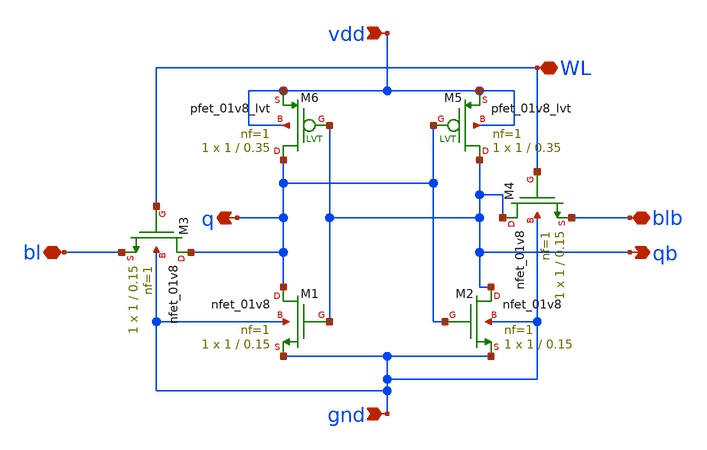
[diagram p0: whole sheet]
** sch_path: sram.sch
**.subckt sram vdd bl q gnd WL blb qb
*.ipin vdd
*.iopin bl
*.opin q
*.ipin gnd
*.iopin WL
*.iopin blb
*.opin qb
XM1 q qb gnd gnd sky130_fd_pr__nfet_01v8 L=0.15 W=1 nf=1 ad='int((nf+1)/2) * W/nf * 0.29' as='int((nf+2)/2) * W/nf * 0.29'
+ pd='2*int((nf+1)/2) * (W/nf + 0.29)' ps='2*int((nf+2)/2) * (W/nf + 0.29)' nrd='0.29 / W' nrs='0.29 / W'
+ sa=0 sb=0 sd=0 mult=1 m=1
XM2 qb q gnd gnd sky130_fd_pr__nfet_01v8 L=0.15 W=1 nf=1 ad='int((nf+1)/2) * W/nf * 0.29' as='int((nf+2)/2) * W/nf * 0.29'
+ pd='2*int((nf+1)/2) * (W/nf + 0.29)' ps='2*int((nf+2)/2) * (W/nf + 0.29)' nrd='0.29 / W' nrs='0.29 / W'
+ sa=0 sb=0 sd=0 mult=1 m=1
XM3 q WL bl gnd sky130_fd_pr__nfet_01v8 L=0.15 W=1 nf=1 ad='int((nf+1)/2) * W/nf * 0.29' as='int((nf+2)/2) * W/nf * 0.29'
+ pd='2*int((nf+1)/2) * (W/nf + 0.29)' ps='2*int((nf+2)/2) * (W/nf + 0.29)' nrd='0.29 / W' nrs='0.29 / W'
+ sa=0 sb=0 sd=0 mult=1 m=1
XM4 qb WL blb gnd sky130_fd_pr__nfet_01v8 L=0.15 W=1 nf=1 ad='int((nf+1)/2) * W/nf * 0.29' as='int((nf+2)/2) * W/nf * 0.29'
+ pd='2*int((nf+1)/2) * (W/nf + 0.29)' ps='2*int((nf+2)/2) * (W/nf + 0.29)' nrd='0.29 / W' nrs='0.29 / W'
+ sa=0 sb=0 sd=0 mult=1 m=1
XM5 qb q vdd vdd sky130_fd_pr__pfet_01v8_lvt L=0.35 W=1 nf=1 ad='int((nf+1)/2) * W/nf * 0.29' as='int((nf+2)/2) * W/nf * 0.29'
+ pd='2*int((nf+1)/2) * (W/nf + 0.29)' ps='2*int((nf+2)/2) * (W/nf + 0.29)' nrd='0.29 / W' nrs='0.29 / W'
+ sa=0 sb=0 sd=0 mult=1 m=1
XM6 q qb vdd vdd sky130_fd_pr__pfet_01v8_lvt L=0.35 W=1 nf=1 ad='int((nf+1)/2) * W/nf * 0.29' as='int((nf+2)/2) * W/nf * 0.29'
+ pd='2*int((nf+1)/2) * (W/nf + 0.29)' ps='2*int((nf+2)/2) * (W/nf + 0.29)' nrd='0.29 / W' nrs='0.29 / W'
+ sa=0 sb=0 sd=0 mult=1 m=1
**.ends
.end
